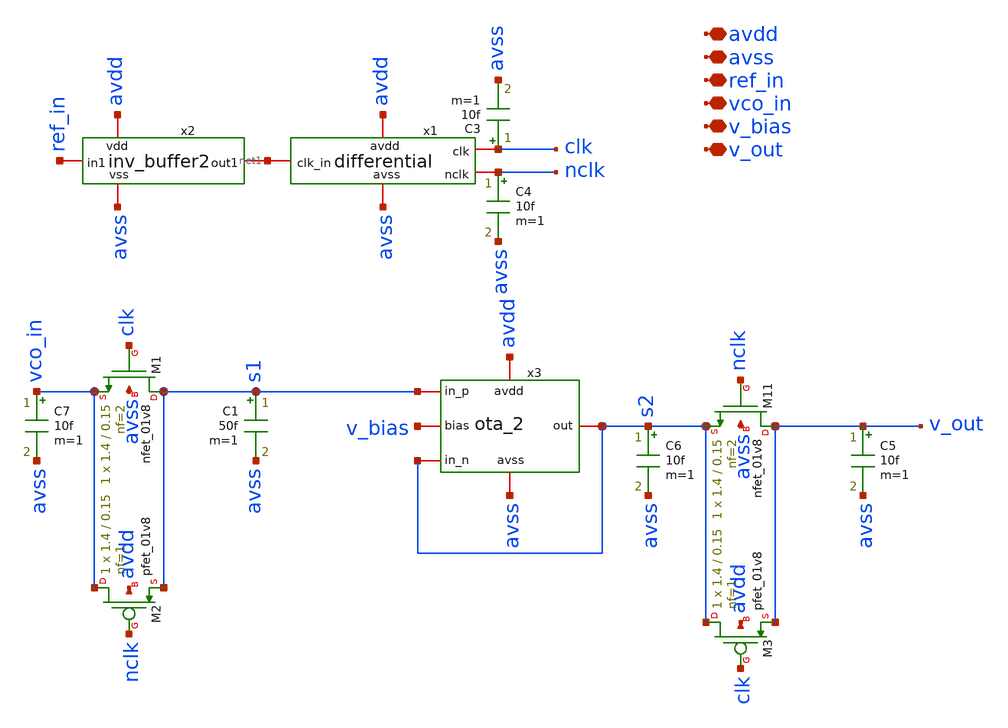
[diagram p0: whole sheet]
** sch_path: xschem/sspd.sch
**.subckt sspd avdd avss ref_in vco_in v_bias v_out
*.iopin avdd
*.iopin avss
*.iopin ref_in
*.iopin vco_in
*.iopin v_bias
*.iopin v_out
x1 avdd avss net1 clk nclk differential
x3 avdd avss s1 s2 s2 v_bias ota_2
C1 s1 avss 50f m=1
XM11 v_out nclk s2 avss sky130_fd_pr__nfet_01v8 L=0.15 W=1.4 nf=2 ad='int((nf+1)/2) * W/nf * 0.29' as='int((nf+2)/2) * W/nf * 0.29'
+ pd='2*int((nf+1)/2) * (W/nf + 0.29)' ps='2*int((nf+2)/2) * (W/nf + 0.29)' nrd='0.29 / W' nrs='0.29 / W'
+ sa=0 sb=0 sd=0 mult=1 m=1
XM1 s1 clk vco_in avss sky130_fd_pr__nfet_01v8 L=0.15 W=1.4 nf=2 ad='int((nf+1)/2) * W/nf * 0.29' as='int((nf+2)/2) * W/nf * 0.29'
+ pd='2*int((nf+1)/2) * (W/nf + 0.29)' ps='2*int((nf+2)/2) * (W/nf + 0.29)' nrd='0.29 / W' nrs='0.29 / W'
+ sa=0 sb=0 sd=0 mult=1 m=1
C3 clk avss 10f m=1
C4 nclk avss 10f m=1
C6 s2 avss 10f m=1
C7 vco_in avss 10f m=1
XM2 vco_in nclk s1 avdd sky130_fd_pr__pfet_01v8 L=0.15 W=1.4 nf=1 ad='int((nf+1)/2) * W/nf * 0.29' as='int((nf+2)/2) * W/nf * 0.29'
+ pd='2*int((nf+1)/2) * (W/nf + 0.29)' ps='2*int((nf+2)/2) * (W/nf + 0.29)' nrd='0.29 / W' nrs='0.29 / W'
+ sa=0 sb=0 sd=0 mult=1 m=1
XM3 s2 clk v_out avdd sky130_fd_pr__pfet_01v8 L=0.15 W=1.4 nf=1 ad='int((nf+1)/2) * W/nf * 0.29' as='int((nf+2)/2) * W/nf * 0.29'
+ pd='2*int((nf+1)/2) * (W/nf + 0.29)' ps='2*int((nf+2)/2) * (W/nf + 0.29)' nrd='0.29 / W' nrs='0.29 / W'
+ sa=0 sb=0 sd=0 mult=1 m=1
C5 v_out avss 10f m=1
x2 avdd avss net1 ref_in inv_buffer2
**.ends
.end
